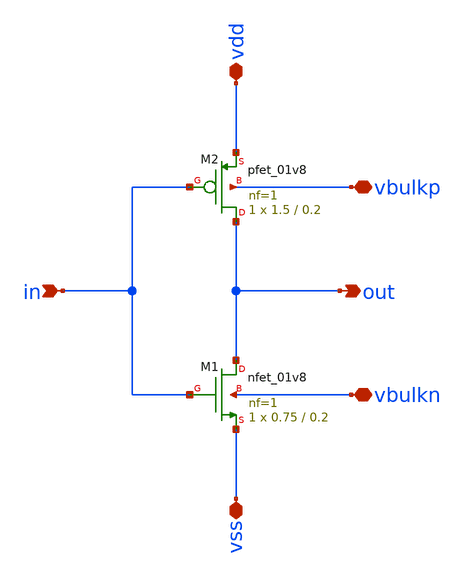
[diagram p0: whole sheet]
** sch_path: xschem/inverter_csvco.sch
**.subckt inverter_csvco vss in out vdd vbulkn vbulkp
*.iopin vss
*.ipin in
*.opin out
*.iopin vdd
*.iopin vbulkn
*.iopin vbulkp
XM1 out in vss vbulkn sky130_fd_pr__nfet_01v8 L=0.2 W=0.75 nf=1 ad='int((nf+1)/2) * W/nf * 0.29' as='int((nf+2)/2) * W/nf * 0.29'
+ pd='2*int((nf+1)/2) * (W/nf + 0.29)' ps='2*int((nf+2)/2) * (W/nf + 0.29)' nrd='0.29 / W' nrs='0.29 / W'
+ sa=0 sb=0 sd=0 mult=1 m=1
XM2 out in vdd vbulkp sky130_fd_pr__pfet_01v8 L=0.2 W=1.5 nf=1 ad='int((nf+1)/2) * W/nf * 0.29' as='int((nf+2)/2) * W/nf * 0.29'
+ pd='2*int((nf+1)/2) * (W/nf + 0.29)' ps='2*int((nf+2)/2) * (W/nf + 0.29)' nrd='0.29 / W' nrs='0.29 / W'
+ sa=0 sb=0 sd=0 mult=1 m=1
**.ends
.end
